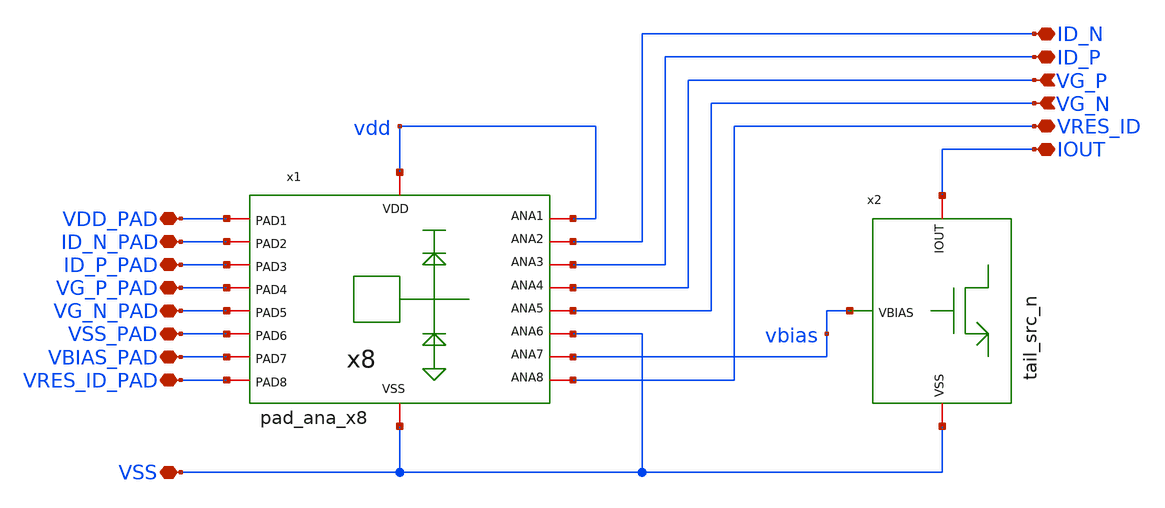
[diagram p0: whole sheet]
** sch_path: xschem/testcells/tb_nmos.sch
**.subckt tb_nmos VDD_PAD ID_N_PAD ID_P_PAD VG_P_PAD VG_N_PAD VSS_PAD VBIAS_PAD VRES_ID_PAD VSS IOUT
*+ VRES_ID ID_N ID_P VG_P VG_N
*.iopin VDD_PAD
*.iopin ID_N_PAD
*.iopin ID_P_PAD
*.iopin VG_P_PAD
*.iopin VG_N_PAD
*.iopin VSS_PAD
*.iopin VBIAS_PAD
*.iopin VRES_ID_PAD
*.iopin VSS
*.iopin IOUT
*.iopin VRES_ID
*.iopin ID_N
*.iopin ID_P
*.ipin VG_P
*.ipin VG_N
x1 VSS_PAD VDD_PAD VG_P_PAD VG_N_PAD ID_N_PAD ID_P_PAD VBIAS_PAD VRES_ID_PAD vdd VSS VG_N VG_P
+ VRES_ID ID_P vbias VSS ID_N vdd pad_ana_x8
x2 IOUT vbias VSS tail_src_n
**.ends
.end
